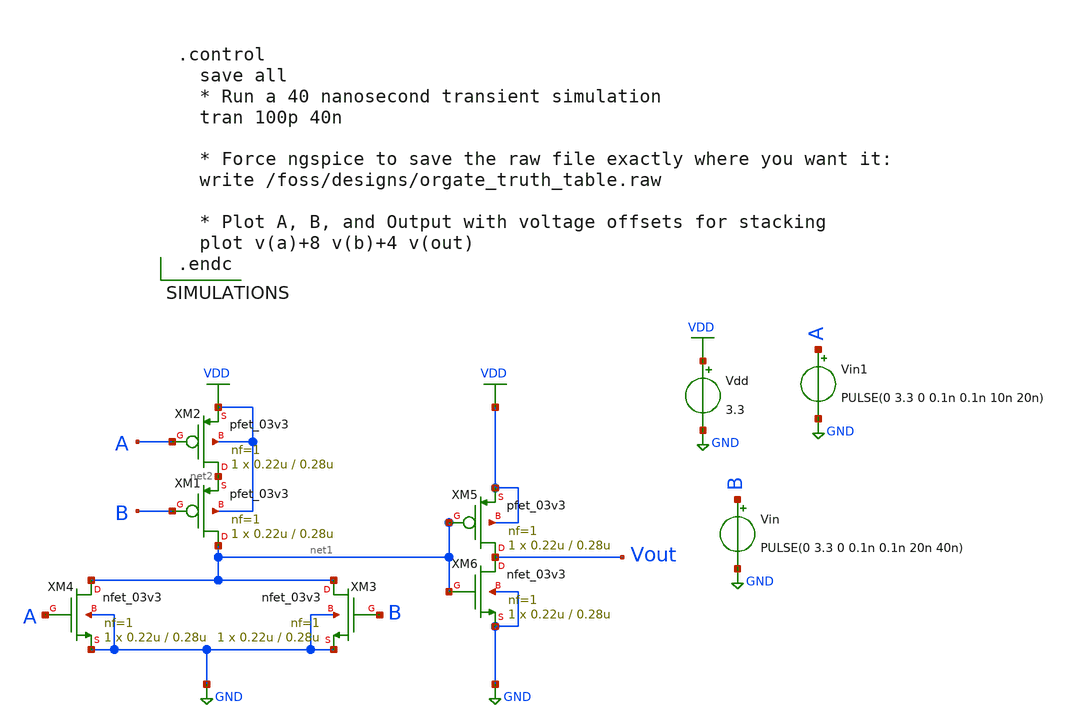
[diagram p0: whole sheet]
** sch_path: OR/or_test.sch
**.subckt or_test
XM2 net2 A VDD VDD pfet_03v3 L=0.28u W=0.22u nf=1 ad='int((nf+1)/2) * W/nf * 0.18u' as='int((nf+2)/2) * W/nf * 0.18u'
+ pd='2*int((nf+1)/2) * (W/nf + 0.18u)' ps='2*int((nf+2)/2) * (W/nf + 0.18u)' nrd='0.18u / W' nrs='0.18u / W'
+ sa=0 sb=0 sd=0 m=1
XM4 net1 A GND GND nfet_03v3 L=0.28u W=0.22u nf=1 ad='int((nf+1)/2) * W/nf * 0.18u' as='int((nf+2)/2) * W/nf * 0.18u'
+ pd='2*int((nf+1)/2) * (W/nf + 0.18u)' ps='2*int((nf+2)/2) * (W/nf + 0.18u)' nrd='0.18u / W' nrs='0.18u / W'
+ sa=0 sb=0 sd=0 m=1
Vdd VDD GND 3.3
Vin B GND PULSE(0 3.3 0 0.1n 0.1n 20n 40n)
Vin1 A GND PULSE(0 3.3 0 0.1n 0.1n 10n 20n)
XM1 net1 B net2 VDD pfet_03v3 L=0.28u W=0.22u nf=1 ad='int((nf+1)/2) * W/nf * 0.18u' as='int((nf+2)/2) * W/nf * 0.18u'
+ pd='2*int((nf+1)/2) * (W/nf + 0.18u)' ps='2*int((nf+2)/2) * (W/nf + 0.18u)' nrd='0.18u / W' nrs='0.18u / W'
+ sa=0 sb=0 sd=0 m=1
XM3 net1 B GND GND nfet_03v3 L=0.28u W=0.22u nf=1 ad='int((nf+1)/2) * W/nf * 0.18u' as='int((nf+2)/2) * W/nf * 0.18u'
+ pd='2*int((nf+1)/2) * (W/nf + 0.18u)' ps='2*int((nf+2)/2) * (W/nf + 0.18u)' nrd='0.18u / W' nrs='0.18u / W'
+ sa=0 sb=0 sd=0 m=1
XM5 Vout net1 VDD VDD pfet_03v3 L=0.28u W=0.22u nf=1 ad='int((nf+1)/2) * W/nf * 0.18u' as='int((nf+2)/2) * W/nf * 0.18u'
+ pd='2*int((nf+1)/2) * (W/nf + 0.18u)' ps='2*int((nf+2)/2) * (W/nf + 0.18u)' nrd='0.18u / W' nrs='0.18u / W'
+ sa=0 sb=0 sd=0 m=1
XM6 Vout net1 GND GND nfet_03v3 L=0.28u W=0.22u nf=1 ad='int((nf+1)/2) * W/nf * 0.18u' as='int((nf+2)/2) * W/nf * 0.18u'
+ pd='2*int((nf+1)/2) * (W/nf + 0.18u)' ps='2*int((nf+2)/2) * (W/nf + 0.18u)' nrd='0.18u / W' nrs='0.18u / W'
+ sa=0 sb=0 sd=0 m=1
**** begin user architecture code


.include /foss/pdks/gf180mcuD/libs.tech/ngspice/design.ngspice
.lib /foss/pdks/gf180mcuD/libs.tech/ngspice/sm141064.ngspice typical




.control
  save all
  * Run a 40 nanosecond transient simulation
  tran 100p 40n

  * Force ngspice to save the raw file exactly where you want it:
  write /foss/designs/orgate_truth_table.raw

  * Plot A, B, and Output with voltage offsets for stacking
  plot v(a)+8 v(b)+4 v(out)
.endc


**** end user architecture code
**.ends
.GLOBAL VDD
.GLOBAL GND
.end
